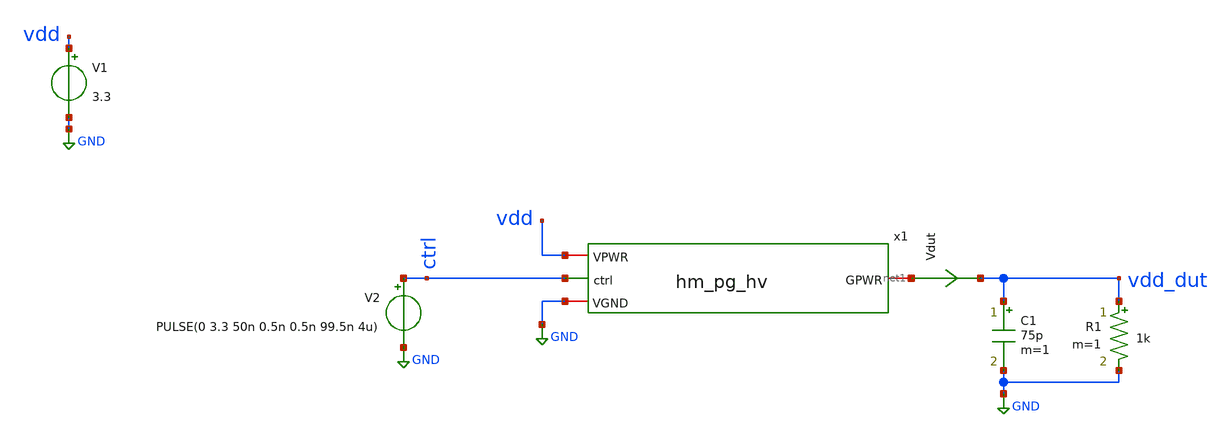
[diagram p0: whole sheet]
** sch_path: ihp-sg13cmos5l/libs.tech/xschem/tests/tb_hm_pg_hv.sch
**.subckt tb_hm_pg_hv
V1 vdd GND 3.3
.save i(v1)
V2 ctrl GND PULSE(0 3.3 50n 0.5n 0.5n 99.5n 4u)
C1 vdd_dut GND 75p m=1
Vdut net1 vdd_dut 0
.save i(vdut)
R1 vdd_dut GND 1k m=1
x1 vdd net1 ctrl GND hm_pg_hv
**** begin user architecture code

.lib cornerMOShv.lib mos_tt
*.lib cornerCAP.lib cap_typ



.param mc_mm_switch=0
.control
save all
tran 50p 5u
plot vdd_dut ctrl
plot vdd_dut x1.ctrl_n ctrl xlimit 50n 58n
*quit 0
.endc
.end


**** end user architecture code
**.ends

* expanding   symbol:
*+  /home/designer/shared/hm-openpdk-library/ihp-sg13cmos5l/libs.tech/xschem/hm_analog/hm_pg_hv.sym # of pins=4
** sym_path: ihp-sg13cmos5l/libs.tech/xschem/hm_analog/hm_pg_hv.sym
** sch_path: ihp-sg13cmos5l/libs.tech/xschem/hm_analog/hm_pg_hv.sch
.subckt hm_pg_hv VPWR GPWR ctrl VGND
*.ipin ctrl
*.iopin VPWR
*.iopin VGND
*.iopin GPWR
XM4 ctrl_n ctrl VGND VGND sg13_hv_nmos w=2.6u l=0.45u ng=1 m=1 mm_ok=1
XM5 ctrl_n ctrl VPWR VPWR sg13_hv_pmos w=4.44u l=0.45u ng=1 m=1 mm_ok=1
XM6 GPWR ctrl_n VPWR VPWR sg13_hv_pmos w=2175u l=0.45u ng=290 m=1 mm_ok=1
.ends

.GLOBAL GND
.end
